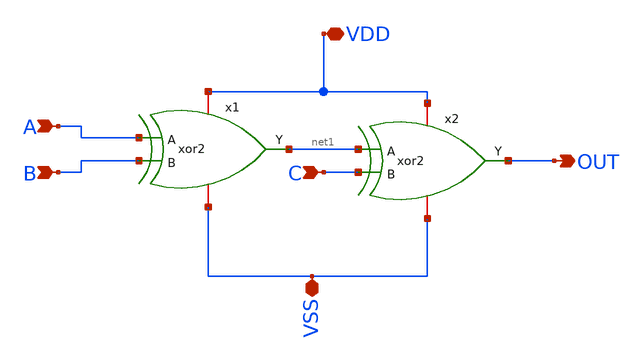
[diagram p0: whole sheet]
** sch_path: design/XOR3/xschem/xor3.sch
**.subckt xor3 C VSS A B OUT VDD
*.ipin C
*.iopin VSS
*.ipin A
*.ipin B
*.opin OUT
*.iopin VDD
x1 net1 A VDD VSS B xor2
x2 OUT net1 VDD VSS C xor2
**.ends
.end
